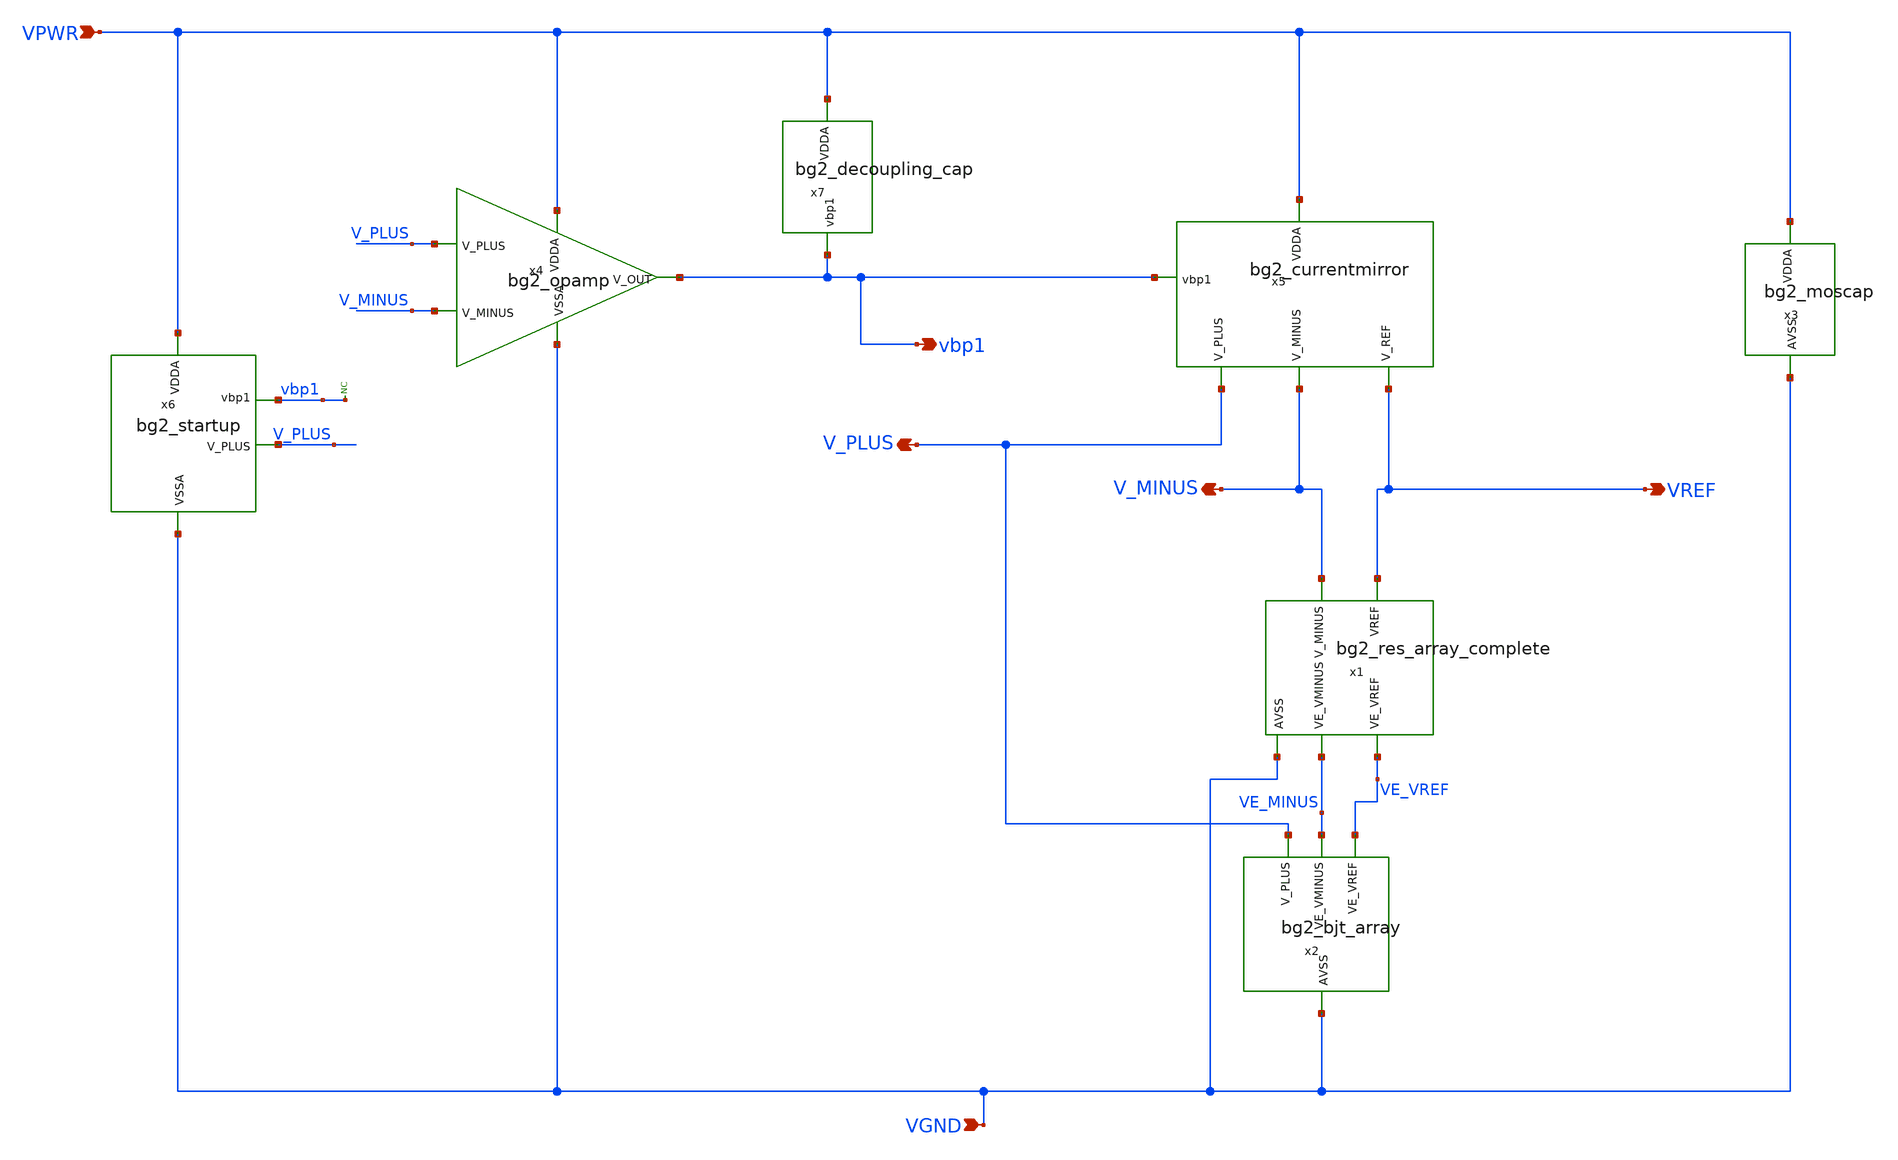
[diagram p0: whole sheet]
** sch_path: lef/lef/lef/gds/bg2_top_tt.sch
**.subckt bg2_top_tt VGND VPWR VREF V_MINUS V_PLUS vbp1
*.ipin VGND
*.ipin VPWR
*.opin VREF
*.opin V_MINUS
*.opin V_PLUS
*.opin vbp1
* noconn vbp1
x7 VPWR vbp1 bg2_decoupling_cap
x6 VPWR vbp1 V_PLUS VGND bg2_startup
x4 VPWR vbp1 V_PLUS V_MINUS VGND bg2_opamp
x5 VPWR vbp1 V_MINUS VREF V_PLUS bg2_currentmirror
x1 V_MINUS VREF VGND VE_VREF VE_MINUS bg2_res_array_complete
x2 V_PLUS VE_MINUS VE_VREF VGND bg2_bjt_array
x3 VPWR VGND bg2_moscap
**.ends
.end
